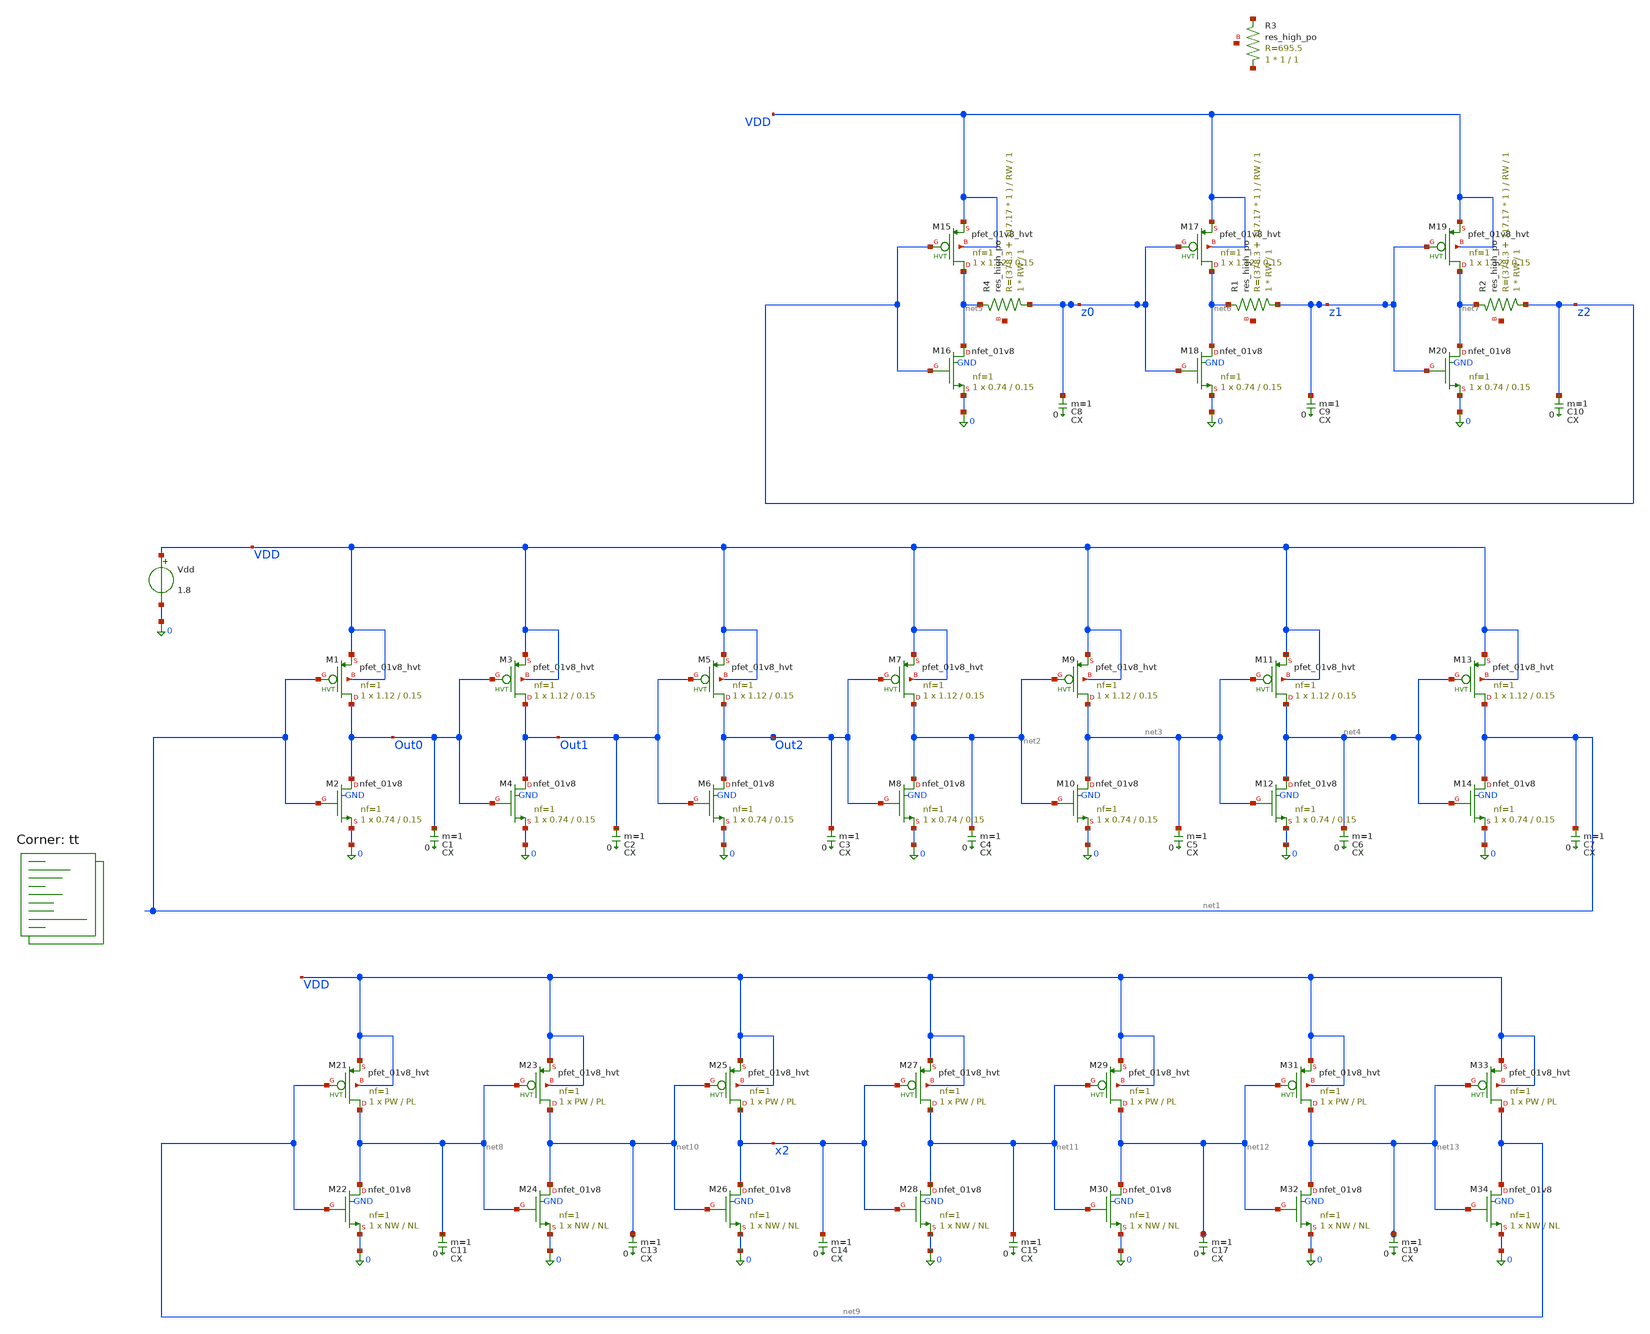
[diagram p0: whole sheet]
** sch_path: schem/ring_osc_freq_response_tb.sch
**.subckt ring_osc_freq_response_tb
XM1 Out0 net1 VDD VDD sky130_fd_pr__pfet_01v8_hvt L=0.15 W=1.12 nf=1 ad='int((1 + 1)/2) * 1.12 / 1 * 0.29'
+ as='int((1 + 2)/2) * 1.12 / 1 * 0.29' pd='2*int((1 + 1)/2) * (1.12 / 1 + 0.29)' ps='2*int((1 + 2)/2) * (1.12 / 1 + 0.29)'
+ nrd='0.29 / 1.12 ' nrs='0.29 / 1.12 ' sa=0 sb=0 sd=0 mult=1 m=1
XM2 Out0 net1 0 GND sky130_fd_pr__nfet_01v8 L=0.15 W=0.74 nf=1 ad='int((1 + 1)/2) * 0.74 / 1 * 0.29'
+ as='int((1 + 2)/2) * 0.74 / 1 * 0.29' pd='2*int((1 + 1)/2) * (0.74 / 1 + 0.29)' ps='2*int((1 + 2)/2) * (0.74 / 1 + 0.29)'
+ nrd='0.29 / 0.74 ' nrs='0.29 / 0.74 ' sa=0 sb=0 sd=0 mult=1 m=1
Vdd VDD 0 1.8
.save i(vdd)
XM3 Out1 Out0 VDD VDD sky130_fd_pr__pfet_01v8_hvt L=0.15 W=1.12 nf=1 ad='int((1 + 1)/2) * 1.12 / 1 * 0.29'
+ as='int((1 + 2)/2) * 1.12 / 1 * 0.29' pd='2*int((1 + 1)/2) * (1.12 / 1 + 0.29)' ps='2*int((1 + 2)/2) * (1.12 / 1 + 0.29)'
+ nrd='0.29 / 1.12 ' nrs='0.29 / 1.12 ' sa=0 sb=0 sd=0 mult=1 m=1
XM4 Out1 Out0 0 GND sky130_fd_pr__nfet_01v8 L=0.15 W=0.74 nf=1 ad='int((1 + 1)/2) * 0.74 / 1 * 0.29'
+ as='int((1 + 2)/2) * 0.74 / 1 * 0.29' pd='2*int((1 + 1)/2) * (0.74 / 1 + 0.29)' ps='2*int((1 + 2)/2) * (0.74 / 1 + 0.29)'
+ nrd='0.29 / 0.74 ' nrs='0.29 / 0.74 ' sa=0 sb=0 sd=0 mult=1 m=1
XM5 Out2 Out1 VDD VDD sky130_fd_pr__pfet_01v8_hvt L=0.15 W=1.12 nf=1 ad='int((1 + 1)/2) * 1.12 / 1 * 0.29'
+ as='int((1 + 2)/2) * 1.12 / 1 * 0.29' pd='2*int((1 + 1)/2) * (1.12 / 1 + 0.29)' ps='2*int((1 + 2)/2) * (1.12 / 1 + 0.29)'
+ nrd='0.29 / 1.12 ' nrs='0.29 / 1.12 ' sa=0 sb=0 sd=0 mult=1 m=1
XM6 Out2 Out1 0 GND sky130_fd_pr__nfet_01v8 L=0.15 W=0.74 nf=1 ad='int((1 + 1)/2) * 0.74 / 1 * 0.29'
+ as='int((1 + 2)/2) * 0.74 / 1 * 0.29' pd='2*int((1 + 1)/2) * (0.74 / 1 + 0.29)' ps='2*int((1 + 2)/2) * (0.74 / 1 + 0.29)'
+ nrd='0.29 / 0.74 ' nrs='0.29 / 0.74 ' sa=0 sb=0 sd=0 mult=1 m=1
XM7 net2 Out2 VDD VDD sky130_fd_pr__pfet_01v8_hvt L=0.15 W=1.12 nf=1 ad='int((1 + 1)/2) * 1.12 / 1 * 0.29'
+ as='int((1 + 2)/2) * 1.12 / 1 * 0.29' pd='2*int((1 + 1)/2) * (1.12 / 1 + 0.29)' ps='2*int((1 + 2)/2) * (1.12 / 1 + 0.29)'
+ nrd='0.29 / 1.12 ' nrs='0.29 / 1.12 ' sa=0 sb=0 sd=0 mult=1 m=1
XM8 net2 Out2 0 GND sky130_fd_pr__nfet_01v8 L=0.15 W=0.74 nf=1 ad='int((1 + 1)/2) * 0.74 / 1 * 0.29'
+ as='int((1 + 2)/2) * 0.74 / 1 * 0.29' pd='2*int((1 + 1)/2) * (0.74 / 1 + 0.29)' ps='2*int((1 + 2)/2) * (0.74 / 1 + 0.29)'
+ nrd='0.29 / 0.74 ' nrs='0.29 / 0.74 ' sa=0 sb=0 sd=0 mult=1 m=1
XM9 net3 net2 VDD VDD sky130_fd_pr__pfet_01v8_hvt L=0.15 W=1.12 nf=1 ad='int((1 + 1)/2) * 1.12 / 1 * 0.29'
+ as='int((1 + 2)/2) * 1.12 / 1 * 0.29' pd='2*int((1 + 1)/2) * (1.12 / 1 + 0.29)' ps='2*int((1 + 2)/2) * (1.12 / 1 + 0.29)'
+ nrd='0.29 / 1.12 ' nrs='0.29 / 1.12 ' sa=0 sb=0 sd=0 mult=1 m=1
XM10 net3 net2 0 GND sky130_fd_pr__nfet_01v8 L=0.15 W=0.74 nf=1 ad='int((1 + 1)/2) * 0.74 / 1 * 0.29'
+ as='int((1 + 2)/2) * 0.74 / 1 * 0.29' pd='2*int((1 + 1)/2) * (0.74 / 1 + 0.29)' ps='2*int((1 + 2)/2) * (0.74 / 1 + 0.29)'
+ nrd='0.29 / 0.74 ' nrs='0.29 / 0.74 ' sa=0 sb=0 sd=0 mult=1 m=1
XM11 net4 net3 VDD VDD sky130_fd_pr__pfet_01v8_hvt L=0.15 W=1.12 nf=1 ad='int((1 + 1)/2) * 1.12 / 1 * 0.29'
+ as='int((1 + 2)/2) * 1.12 / 1 * 0.29' pd='2*int((1 + 1)/2) * (1.12 / 1 + 0.29)' ps='2*int((1 + 2)/2) * (1.12 / 1 + 0.29)'
+ nrd='0.29 / 1.12 ' nrs='0.29 / 1.12 ' sa=0 sb=0 sd=0 mult=1 m=1
XM12 net4 net3 0 GND sky130_fd_pr__nfet_01v8 L=0.15 W=0.74 nf=1 ad='int((1 + 1)/2) * 0.74 / 1 * 0.29'
+ as='int((1 + 2)/2) * 0.74 / 1 * 0.29' pd='2*int((1 + 1)/2) * (0.74 / 1 + 0.29)' ps='2*int((1 + 2)/2) * (0.74 / 1 + 0.29)'
+ nrd='0.29 / 0.74 ' nrs='0.29 / 0.74 ' sa=0 sb=0 sd=0 mult=1 m=1
XM13 net1 net4 VDD VDD sky130_fd_pr__pfet_01v8_hvt L=0.15 W=1.12 nf=1 ad='int((1 + 1)/2) * 1.12 / 1 * 0.29'
+ as='int((1 + 2)/2) * 1.12 / 1 * 0.29' pd='2*int((1 + 1)/2) * (1.12 / 1 + 0.29)' ps='2*int((1 + 2)/2) * (1.12 / 1 + 0.29)'
+ nrd='0.29 / 1.12 ' nrs='0.29 / 1.12 ' sa=0 sb=0 sd=0 mult=1 m=1
XM14 net1 net4 0 GND sky130_fd_pr__nfet_01v8 L=0.15 W=0.74 nf=1 ad='int((1 + 1)/2) * 0.74 / 1 * 0.29'
+ as='int((1 + 2)/2) * 0.74 / 1 * 0.29' pd='2*int((1 + 1)/2) * (0.74 / 1 + 0.29)' ps='2*int((1 + 2)/2) * (0.74 / 1 + 0.29)'
+ nrd='0.29 / 0.74 ' nrs='0.29 / 0.74 ' sa=0 sb=0 sd=0 mult=1 m=1
C1 Out0 0 CX m=1
C2 Out1 0 CX m=1
C3 Out2 0 CX m=1
C4 net2 0 CX m=1
C5 net3 0 CX m=1
C6 net4 0 CX m=1
C7 net1 0 CX m=1
XM15 net5 z2 VDD VDD sky130_fd_pr__pfet_01v8_hvt L=0.15 W=1.12 nf=1 ad='int((1 + 1)/2) * 1.12 / 1 * 0.29'
+ as='int((1 + 2)/2) * 1.12 / 1 * 0.29' pd='2*int((1 + 1)/2) * (1.12 / 1 + 0.29)' ps='2*int((1 + 2)/2) * (1.12 / 1 + 0.29)'
+ nrd='0.29 / 1.12 ' nrs='0.29 / 1.12 ' sa=0 sb=0 sd=0 mult=1 m=1
XM16 net5 z2 0 GND sky130_fd_pr__nfet_01v8 L=0.15 W=0.74 nf=1 ad='int((1 + 1)/2) * 0.74 / 1 * 0.29' as='int((1 + 2)/2) * 0.74 / 1 * 0.29'
+ pd='2*int((1 + 1)/2) * (0.74 / 1 + 0.29)' ps='2*int((1 + 2)/2) * (0.74 / 1 + 0.29)' nrd='0.29 / 0.74 '
+ nrs='0.29 / 0.74 ' sa=0 sb=0 sd=0 mult=1 m=1
C8 z0 0 CX m=1
XM17 net6 z0 VDD VDD sky130_fd_pr__pfet_01v8_hvt L=0.15 W=1.12 nf=1 ad='int((1 + 1)/2) * 1.12 / 1 * 0.29'
+ as='int((1 + 2)/2) * 1.12 / 1 * 0.29' pd='2*int((1 + 1)/2) * (1.12 / 1 + 0.29)' ps='2*int((1 + 2)/2) * (1.12 / 1 + 0.29)'
+ nrd='0.29 / 1.12 ' nrs='0.29 / 1.12 ' sa=0 sb=0 sd=0 mult=1 m=1
XM18 net6 z0 0 GND sky130_fd_pr__nfet_01v8 L=0.15 W=0.74 nf=1 ad='int((1 + 1)/2) * 0.74 / 1 * 0.29' as='int((1 + 2)/2) * 0.74 / 1 * 0.29'
+ pd='2*int((1 + 1)/2) * (0.74 / 1 + 0.29)' ps='2*int((1 + 2)/2) * (0.74 / 1 + 0.29)' nrd='0.29 / 0.74 '
+ nrs='0.29 / 0.74 ' sa=0 sb=0 sd=0 mult=1 m=1
C9 z1 0 CX m=1
XM19 net7 z1 VDD VDD sky130_fd_pr__pfet_01v8_hvt L=0.15 W=1.12 nf=1 ad='int((1 + 1)/2) * 1.12 / 1 * 0.29'
+ as='int((1 + 2)/2) * 1.12 / 1 * 0.29' pd='2*int((1 + 1)/2) * (1.12 / 1 + 0.29)' ps='2*int((1 + 2)/2) * (1.12 / 1 + 0.29)'
+ nrd='0.29 / 1.12 ' nrs='0.29 / 1.12 ' sa=0 sb=0 sd=0 mult=1 m=1
XM20 net7 z1 0 GND sky130_fd_pr__nfet_01v8 L=0.15 W=0.74 nf=1 ad='int((1 + 1)/2) * 0.74 / 1 * 0.29' as='int((1 + 2)/2) * 0.74 / 1 * 0.29'
+ pd='2*int((1 + 1)/2) * (0.74 / 1 + 0.29)' ps='2*int((1 + 2)/2) * (0.74 / 1 + 0.29)' nrd='0.29 / 0.74 '
+ nrs='0.29 / 0.74 ' sa=0 sb=0 sd=0 mult=1 m=1
C10 z2 0 CX m=1
XR4 z0 net5 net14 sky130_fd_pr__res_high_po W=RW L=1 mult=1 m=1
XR1 z1 net6 net15 sky130_fd_pr__res_high_po W=RW L=1 mult=1 m=1
XR2 z2 net7 net16 sky130_fd_pr__res_high_po W=RW L=1 mult=1 m=1
XR3 net17 net18 net19 sky130_fd_pr__res_high_po W=1 L=1 mult=1 m=1
XM21 net8 net9 VDD VDD sky130_fd_pr__pfet_01v8_hvt L=PL W=PW nf=1 ad='int((1 + 1)/2) * PW / 1 * 0.29'
+ as='int((1 + 2)/2) * PW / 1 * 0.29' pd='2*int((1 + 1)/2) * (PW / 1 + 0.29)' ps='2*int((1 + 2)/2) * (PW / 1 + 0.29)'
+ nrd='0.29 / PW ' nrs='0.29 / PW ' sa=0 sb=0 sd=0 mult=1 m=1
XM22 net8 net9 0 GND sky130_fd_pr__nfet_01v8 L=NL W=NW nf=1 ad='int((1 + 1)/2) * NW / 1 * 0.29' as='int((1 + 2)/2) * NW / 1 * 0.29'
+ pd='2*int((1 + 1)/2) * (NW / 1 + 0.29)' ps='2*int((1 + 2)/2) * (NW / 1 + 0.29)' nrd='0.29 / NW ' nrs='0.29 / NW '
+ sa=0 sb=0 sd=0 mult=1 m=1
C11 net8 0 CX m=1
XM23 net10 net8 VDD VDD sky130_fd_pr__pfet_01v8_hvt L=PL W=PW nf=1 ad='int((1 + 1)/2) * PW / 1 * 0.29'
+ as='int((1 + 2)/2) * PW / 1 * 0.29' pd='2*int((1 + 1)/2) * (PW / 1 + 0.29)' ps='2*int((1 + 2)/2) * (PW / 1 + 0.29)'
+ nrd='0.29 / PW ' nrs='0.29 / PW ' sa=0 sb=0 sd=0 mult=1 m=1
XM24 net10 net8 0 GND sky130_fd_pr__nfet_01v8 L=NL W=NW nf=1 ad='int((1 + 1)/2) * NW / 1 * 0.29' as='int((1 + 2)/2) * NW / 1 * 0.29'
+ pd='2*int((1 + 1)/2) * (NW / 1 + 0.29)' ps='2*int((1 + 2)/2) * (NW / 1 + 0.29)' nrd='0.29 / NW ' nrs='0.29 / NW '
+ sa=0 sb=0 sd=0 mult=1 m=1
C13 net10 0 CX m=1
XM25 x2 net10 VDD VDD sky130_fd_pr__pfet_01v8_hvt L=PL W=PW nf=1 ad='int((1 + 1)/2) * PW / 1 * 0.29'
+ as='int((1 + 2)/2) * PW / 1 * 0.29' pd='2*int((1 + 1)/2) * (PW / 1 + 0.29)' ps='2*int((1 + 2)/2) * (PW / 1 + 0.29)'
+ nrd='0.29 / PW ' nrs='0.29 / PW ' sa=0 sb=0 sd=0 mult=1 m=1
XM26 x2 net10 0 GND sky130_fd_pr__nfet_01v8 L=NL W=NW nf=1 ad='int((1 + 1)/2) * NW / 1 * 0.29' as='int((1 + 2)/2) * NW / 1 * 0.29'
+ pd='2*int((1 + 1)/2) * (NW / 1 + 0.29)' ps='2*int((1 + 2)/2) * (NW / 1 + 0.29)' nrd='0.29 / NW ' nrs='0.29 / NW '
+ sa=0 sb=0 sd=0 mult=1 m=1
C14 x2 0 CX m=1
XM27 net11 x2 VDD VDD sky130_fd_pr__pfet_01v8_hvt L=PL W=PW nf=1 ad='int((1 + 1)/2) * PW / 1 * 0.29'
+ as='int((1 + 2)/2) * PW / 1 * 0.29' pd='2*int((1 + 1)/2) * (PW / 1 + 0.29)' ps='2*int((1 + 2)/2) * (PW / 1 + 0.29)'
+ nrd='0.29 / PW ' nrs='0.29 / PW ' sa=0 sb=0 sd=0 mult=1 m=1
XM28 net11 x2 0 GND sky130_fd_pr__nfet_01v8 L=NL W=NW nf=1 ad='int((1 + 1)/2) * NW / 1 * 0.29' as='int((1 + 2)/2) * NW / 1 * 0.29'
+ pd='2*int((1 + 1)/2) * (NW / 1 + 0.29)' ps='2*int((1 + 2)/2) * (NW / 1 + 0.29)' nrd='0.29 / NW ' nrs='0.29 / NW '
+ sa=0 sb=0 sd=0 mult=1 m=1
C15 net11 0 CX m=1
XM29 net12 net11 VDD VDD sky130_fd_pr__pfet_01v8_hvt L=PL W=PW nf=1 ad='int((1 + 1)/2) * PW / 1 * 0.29'
+ as='int((1 + 2)/2) * PW / 1 * 0.29' pd='2*int((1 + 1)/2) * (PW / 1 + 0.29)' ps='2*int((1 + 2)/2) * (PW / 1 + 0.29)'
+ nrd='0.29 / PW ' nrs='0.29 / PW ' sa=0 sb=0 sd=0 mult=1 m=1
XM30 net12 net11 0 GND sky130_fd_pr__nfet_01v8 L=NL W=NW nf=1 ad='int((1 + 1)/2) * NW / 1 * 0.29' as='int((1 + 2)/2) * NW / 1 * 0.29'
+ pd='2*int((1 + 1)/2) * (NW / 1 + 0.29)' ps='2*int((1 + 2)/2) * (NW / 1 + 0.29)' nrd='0.29 / NW ' nrs='0.29 / NW '
+ sa=0 sb=0 sd=0 mult=1 m=1
C17 net12 0 CX m=1
XM31 net13 net12 VDD VDD sky130_fd_pr__pfet_01v8_hvt L=PL W=PW nf=1 ad='int((1 + 1)/2) * PW / 1 * 0.29'
+ as='int((1 + 2)/2) * PW / 1 * 0.29' pd='2*int((1 + 1)/2) * (PW / 1 + 0.29)' ps='2*int((1 + 2)/2) * (PW / 1 + 0.29)'
+ nrd='0.29 / PW ' nrs='0.29 / PW ' sa=0 sb=0 sd=0 mult=1 m=1
XM32 net13 net12 0 GND sky130_fd_pr__nfet_01v8 L=NL W=NW nf=1 ad='int((1 + 1)/2) * NW / 1 * 0.29' as='int((1 + 2)/2) * NW / 1 * 0.29'
+ pd='2*int((1 + 1)/2) * (NW / 1 + 0.29)' ps='2*int((1 + 2)/2) * (NW / 1 + 0.29)' nrd='0.29 / NW ' nrs='0.29 / NW '
+ sa=0 sb=0 sd=0 mult=1 m=1
C19 net13 0 CX m=1
XM33 net9 net13 VDD VDD sky130_fd_pr__pfet_01v8_hvt L=PL W=PW nf=1 ad='int((1 + 1)/2) * PW / 1 * 0.29'
+ as='int((1 + 2)/2) * PW / 1 * 0.29' pd='2*int((1 + 1)/2) * (PW / 1 + 0.29)' ps='2*int((1 + 2)/2) * (PW / 1 + 0.29)'
+ nrd='0.29 / PW ' nrs='0.29 / PW ' sa=0 sb=0 sd=0 mult=1 m=1
XM34 net9 net13 0 GND sky130_fd_pr__nfet_01v8 L=NL W=NW nf=1 ad='int((1 + 1)/2) * NW / 1 * 0.29' as='int((1 + 2)/2) * NW / 1 * 0.29'
+ pd='2*int((1 + 1)/2) * (NW / 1 + 0.29)' ps='2*int((1 + 2)/2) * (NW / 1 + 0.29)' nrd='0.29 / NW ' nrs='0.29 / NW '
+ sa=0 sb=0 sd=0 mult=1 m=1
**** begin user architecture code
.lib $::SKYWATER_MODELS/sky130.lib.spice tt



.include ring_osc_freq_response_tb.save
* 320 MHz : RW=1 PW=1.12 PL=0.45 NW=0.740 NL=0.45
* 250 MHz : PW=1.12 PL=0.5 NW=0.82 NL=0.5
* 260 MHz : PW=0.82 PL=0.5 NW=0.55 NL=0.5
* 100 MHz : PW=1.5 PL=1.0 NW=1.0 NL=1.0
* 18 MHz : PW=7.0 PL=0.25 NW=1.0 NL=8.0
.param RW=1
.param CX=64f PW=2.0 PL=1.0 NW=1.0 NL=1.0
.save all
.control
  save all
  tran 1n 1000n
  fft out2 z2 x2
  write slower.raw
  set appendwrite
.endc



**** end user architecture code
**.ends
.end
